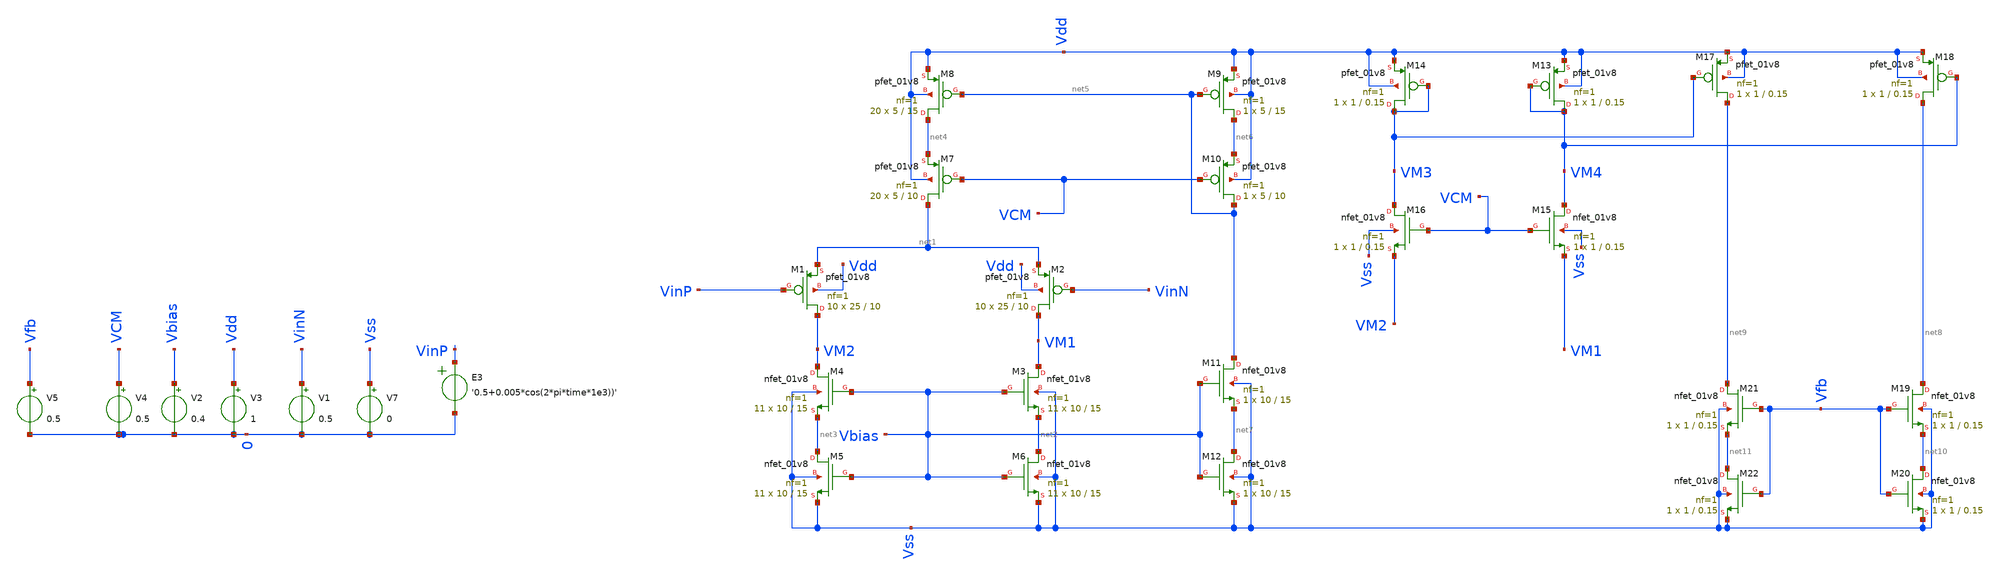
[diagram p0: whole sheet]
** sch_path: Stefan_LNA_core1.sch
**.subckt Stefan_LNA_core1
XM1 VM2 VinP net1 Vdd sky130_fd_pr__pfet_01v8 L=10 W=25 nf=1 ad='int((nf+1)/2) * W/nf * 0.29' as='int((nf+2)/2) * W/nf * 0.29'
+ pd='2*int((nf+1)/2) * (W/nf + 0.29)' ps='2*int((nf+2)/2) * (W/nf + 0.29)' nrd='0.29 / W' nrs='0.29 / W'
+ sa=0 sb=0 sd=0 mult=10 m=10
XM2 VM1 VinN net1 Vdd sky130_fd_pr__pfet_01v8 L=10 W=25 nf=1 ad='int((nf+1)/2) * W/nf * 0.29' as='int((nf+2)/2) * W/nf * 0.29'
+ pd='2*int((nf+1)/2) * (W/nf + 0.29)' ps='2*int((nf+2)/2) * (W/nf + 0.29)' nrd='0.29 / W' nrs='0.29 / W'
+ sa=0 sb=0 sd=0 mult=10 m=10
XM3 VM1 Vbias net2 Vss sky130_fd_pr__nfet_01v8 L=15 W=10 nf=1 ad='int((nf+1)/2) * W/nf * 0.29' as='int((nf+2)/2) * W/nf * 0.29'
+ pd='2*int((nf+1)/2) * (W/nf + 0.29)' ps='2*int((nf+2)/2) * (W/nf + 0.29)' nrd='0.29 / W' nrs='0.29 / W'
+ sa=0 sb=0 sd=0 mult=11 m=11
XM4 VM2 Vbias net3 Vss sky130_fd_pr__nfet_01v8 L=15 W=10 nf=1 ad='int((nf+1)/2) * W/nf * 0.29' as='int((nf+2)/2) * W/nf * 0.29'
+ pd='2*int((nf+1)/2) * (W/nf + 0.29)' ps='2*int((nf+2)/2) * (W/nf + 0.29)' nrd='0.29 / W' nrs='0.29 / W'
+ sa=0 sb=0 sd=0 mult=11 m=11
XM5 net3 Vbias Vss Vss sky130_fd_pr__nfet_01v8 L=15 W=10 nf=1 ad='int((nf+1)/2) * W/nf * 0.29' as='int((nf+2)/2) * W/nf * 0.29'
+ pd='2*int((nf+1)/2) * (W/nf + 0.29)' ps='2*int((nf+2)/2) * (W/nf + 0.29)' nrd='0.29 / W' nrs='0.29 / W'
+ sa=0 sb=0 sd=0 mult=11 m=11
XM6 net2 Vbias Vss Vss sky130_fd_pr__nfet_01v8 L=15 W=10 nf=1 ad='int((nf+1)/2) * W/nf * 0.29' as='int((nf+2)/2) * W/nf * 0.29'
+ pd='2*int((nf+1)/2) * (W/nf + 0.29)' ps='2*int((nf+2)/2) * (W/nf + 0.29)' nrd='0.29 / W' nrs='0.29 / W'
+ sa=0 sb=0 sd=0 mult=11 m=11
XM7 net1 VCM net4 Vdd sky130_fd_pr__pfet_01v8 L=10 W=5 nf=1 ad='int((nf+1)/2) * W/nf * 0.29' as='int((nf+2)/2) * W/nf * 0.29'
+ pd='2*int((nf+1)/2) * (W/nf + 0.29)' ps='2*int((nf+2)/2) * (W/nf + 0.29)' nrd='0.29 / W' nrs='0.29 / W'
+ sa=0 sb=0 sd=0 mult=20 m=20
XM8 net4 net5 Vdd Vdd sky130_fd_pr__pfet_01v8 L=15 W=5 nf=1 ad='int((nf+1)/2) * W/nf * 0.29' as='int((nf+2)/2) * W/nf * 0.29'
+ pd='2*int((nf+1)/2) * (W/nf + 0.29)' ps='2*int((nf+2)/2) * (W/nf + 0.29)' nrd='0.29 / W' nrs='0.29 / W'
+ sa=0 sb=0 sd=0 mult=20 m=20
XM9 net6 net5 Vdd Vdd sky130_fd_pr__pfet_01v8 L=15 W=5 nf=1 ad='int((nf+1)/2) * W/nf * 0.29' as='int((nf+2)/2) * W/nf * 0.29'
+ pd='2*int((nf+1)/2) * (W/nf + 0.29)' ps='2*int((nf+2)/2) * (W/nf + 0.29)' nrd='0.29 / W' nrs='0.29 / W'
+ sa=0 sb=0 sd=0 mult=1 m=1
XM10 net5 VCM net6 Vdd sky130_fd_pr__pfet_01v8 L=10 W=5 nf=1 ad='int((nf+1)/2) * W/nf * 0.29' as='int((nf+2)/2) * W/nf * 0.29'
+ pd='2*int((nf+1)/2) * (W/nf + 0.29)' ps='2*int((nf+2)/2) * (W/nf + 0.29)' nrd='0.29 / W' nrs='0.29 / W'
+ sa=0 sb=0 sd=0 mult=1 m=1
XM11 net5 Vbias net7 Vss sky130_fd_pr__nfet_01v8 L=15 W=10 nf=1 ad='int((nf+1)/2) * W/nf * 0.29' as='int((nf+2)/2) * W/nf * 0.29'
+ pd='2*int((nf+1)/2) * (W/nf + 0.29)' ps='2*int((nf+2)/2) * (W/nf + 0.29)' nrd='0.29 / W' nrs='0.29 / W'
+ sa=0 sb=0 sd=0 mult=1 m=1
XM12 net7 Vbias Vss Vss sky130_fd_pr__nfet_01v8 L=15 W=10 nf=1 ad='int((nf+1)/2) * W/nf * 0.29' as='int((nf+2)/2) * W/nf * 0.29'
+ pd='2*int((nf+1)/2) * (W/nf + 0.29)' ps='2*int((nf+2)/2) * (W/nf + 0.29)' nrd='0.29 / W' nrs='0.29 / W'
+ sa=0 sb=0 sd=0 mult=1 m=1
XM13 VM4 VM4 Vdd Vdd sky130_fd_pr__pfet_01v8 L=0.15 W=1 nf=1 ad='int((nf+1)/2) * W/nf * 0.29' as='int((nf+2)/2) * W/nf * 0.29'
+ pd='2*int((nf+1)/2) * (W/nf + 0.29)' ps='2*int((nf+2)/2) * (W/nf + 0.29)' nrd='0.29 / W' nrs='0.29 / W'
+ sa=0 sb=0 sd=0 mult=1 m=1
XM14 VM3 VM3 Vdd Vdd sky130_fd_pr__pfet_01v8 L=0.15 W=1 nf=1 ad='int((nf+1)/2) * W/nf * 0.29' as='int((nf+2)/2) * W/nf * 0.29'
+ pd='2*int((nf+1)/2) * (W/nf + 0.29)' ps='2*int((nf+2)/2) * (W/nf + 0.29)' nrd='0.29 / W' nrs='0.29 / W'
+ sa=0 sb=0 sd=0 mult=1 m=1
XM15 VM4 VCM VM1 Vss sky130_fd_pr__nfet_01v8 L=0.15 W=1 nf=1 ad='int((nf+1)/2) * W/nf * 0.29' as='int((nf+2)/2) * W/nf * 0.29'
+ pd='2*int((nf+1)/2) * (W/nf + 0.29)' ps='2*int((nf+2)/2) * (W/nf + 0.29)' nrd='0.29 / W' nrs='0.29 / W'
+ sa=0 sb=0 sd=0 mult=1 m=1
XM16 VM3 VCM VM2 Vss sky130_fd_pr__nfet_01v8 L=0.15 W=1 nf=1 ad='int((nf+1)/2) * W/nf * 0.29' as='int((nf+2)/2) * W/nf * 0.29'
+ pd='2*int((nf+1)/2) * (W/nf + 0.29)' ps='2*int((nf+2)/2) * (W/nf + 0.29)' nrd='0.29 / W' nrs='0.29 / W'
+ sa=0 sb=0 sd=0 mult=1 m=1
XM17 net9 VM3 Vdd Vdd sky130_fd_pr__pfet_01v8 L=0.15 W=1 nf=1 ad='int((nf+1)/2) * W/nf * 0.29' as='int((nf+2)/2) * W/nf * 0.29'
+ pd='2*int((nf+1)/2) * (W/nf + 0.29)' ps='2*int((nf+2)/2) * (W/nf + 0.29)' nrd='0.29 / W' nrs='0.29 / W'
+ sa=0 sb=0 sd=0 mult=1 m=1
XM18 net8 VM4 Vdd Vdd sky130_fd_pr__pfet_01v8 L=0.15 W=1 nf=1 ad='int((nf+1)/2) * W/nf * 0.29' as='int((nf+2)/2) * W/nf * 0.29'
+ pd='2*int((nf+1)/2) * (W/nf + 0.29)' ps='2*int((nf+2)/2) * (W/nf + 0.29)' nrd='0.29 / W' nrs='0.29 / W'
+ sa=0 sb=0 sd=0 mult=1 m=1
XM19 net8 Vfb net10 Vss sky130_fd_pr__nfet_01v8 L=0.15 W=1 nf=1 ad='int((nf+1)/2) * W/nf * 0.29' as='int((nf+2)/2) * W/nf * 0.29'
+ pd='2*int((nf+1)/2) * (W/nf + 0.29)' ps='2*int((nf+2)/2) * (W/nf + 0.29)' nrd='0.29 / W' nrs='0.29 / W'
+ sa=0 sb=0 sd=0 mult=1 m=1
XM20 net10 Vfb Vss Vss sky130_fd_pr__nfet_01v8 L=0.15 W=1 nf=1 ad='int((nf+1)/2) * W/nf * 0.29' as='int((nf+2)/2) * W/nf * 0.29'
+ pd='2*int((nf+1)/2) * (W/nf + 0.29)' ps='2*int((nf+2)/2) * (W/nf + 0.29)' nrd='0.29 / W' nrs='0.29 / W'
+ sa=0 sb=0 sd=0 mult=1 m=1
XM21 net9 Vfb net11 Vss sky130_fd_pr__nfet_01v8 L=0.15 W=1 nf=1 ad='int((nf+1)/2) * W/nf * 0.29' as='int((nf+2)/2) * W/nf * 0.29'
+ pd='2*int((nf+1)/2) * (W/nf + 0.29)' ps='2*int((nf+2)/2) * (W/nf + 0.29)' nrd='0.29 / W' nrs='0.29 / W'
+ sa=0 sb=0 sd=0 mult=1 m=1
XM22 net11 Vfb Vss Vss sky130_fd_pr__nfet_01v8 L=0.15 W=1 nf=1 ad='int((nf+1)/2) * W/nf * 0.29' as='int((nf+2)/2) * W/nf * 0.29'
+ pd='2*int((nf+1)/2) * (W/nf + 0.29)' ps='2*int((nf+2)/2) * (W/nf + 0.29)' nrd='0.29 / W' nrs='0.29 / W'
+ sa=0 sb=0 sd=0 mult=1 m=1
E3 VinP 0 VOL=' '0.5+0.005*cos(2*pi*time*1e3))' '
V3 Vdd 0 1
V7 Vss 0 0
V1 VinN 0 0.5
V2 Vbias 0 0.4
V4 VCM 0 0.5
V5 Vfb 0 0.5
**** begin user architecture code
.lib $::SKYWATER_MODELS/sky130.lib.spice tt

.save all
.tran 0.1u 1m


**** end user architecture code
**.ends
.end
